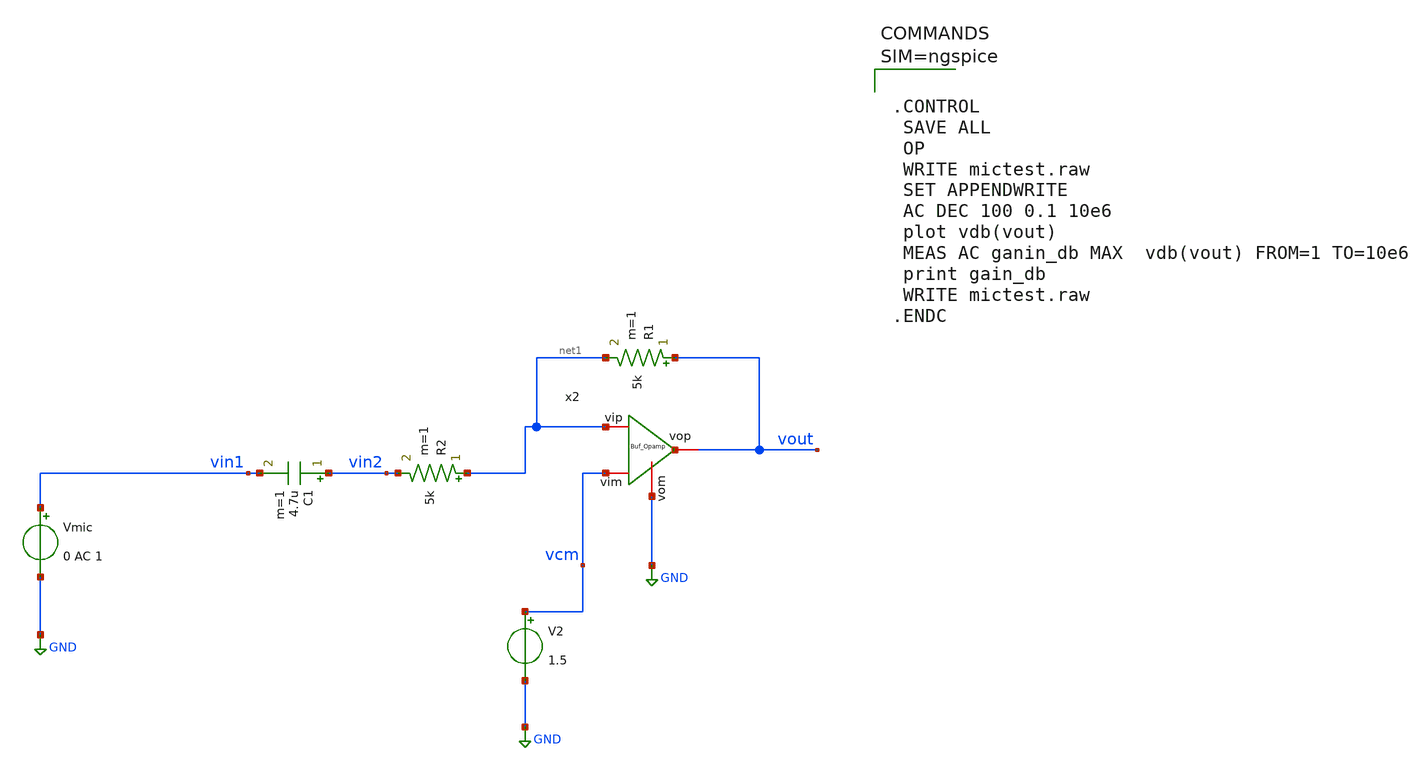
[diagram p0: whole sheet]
** sch_path: xschem/hpassbuff_op.sch
**.subckt hpassbuff_op
Vmic vin1 GND 0 AC 1
C1 vin2 vin1 4.7u m=1
R2 net1 vin2 5k m=1
R1 vout net1 5k m=1
V2 vcm GND 1.5
x2 vout net1 vcm GND Buf_Opamp
**** begin user architecture code



.CONTROL
 SAVE ALL
 OP
 WRITE mictest.raw
 SET APPENDWRITE
 AC DEC 100 0.1 10e6
 plot vdb(vout)
 MEAS AC ganin_db MAX  vdb(vout) FROM=1 TO=10e6
 print gain_db
 WRITE mictest.raw
.ENDC



**** end user architecture code
**.ends
.GLOBAL GND
.end
